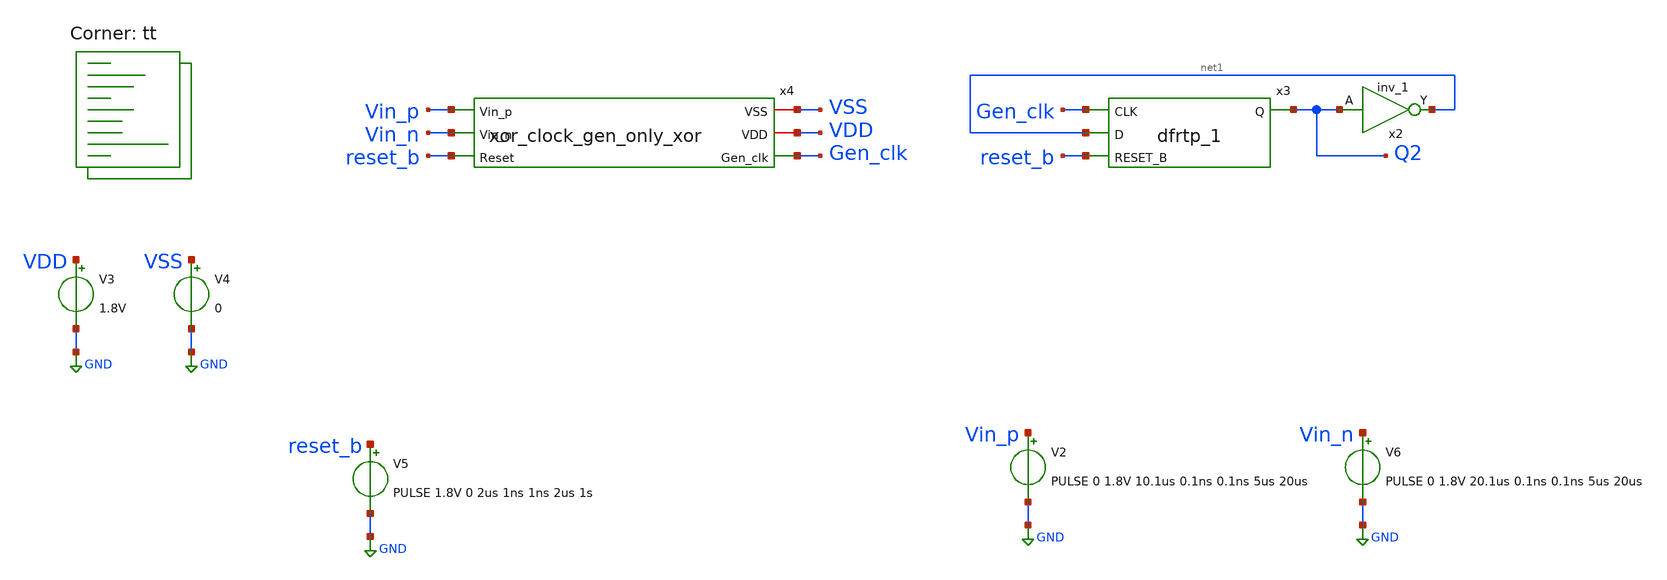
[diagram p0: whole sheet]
** sch_path: xschem/tests/xor_clock_gen/xor_clock_gen__only_xor_test.sch
**.subckt xor_clock_gen__only_xor_test
V3 VDD GND 1.8V
V4 VSS GND 0
V5 reset_b GND PULSE 1.8V 0 2us 1ns 1ns 2us 1s
V2 Vin_p GND PULSE 0 1.8V 10.1us 0.1ns 0.1ns 5us 20us
V6 Vin_n GND PULSE 0 1.8V 20.1us 0.1ns 0.1ns 5us 20us
x3 Gen_clk net1 reset_b VSS VSS VDD VDD Q2 sky130_fd_sc_hd__dfrtp_1
x2 Q2 VSS VSS VDD VDD net1 sky130_fd_sc_hd__inv_1
x4 VSS Vin_p VDD Vin_n Gen_clk reset_b xor_clock_gen_only_xor
**** begin user architecture code
 *.lib $::SKYWATER_MODELS/sky130.lib.spice tt
.include $::SKYWATER_STDCELLS/sky130_fd_sc_hd.spice


.options acct list
.temp 25
*vvcc VDD 0 dc 1.8
*vvss VSS 0 0
.control
save all
tran 0.01u 80u
*plot RST_PLS clk+2 Pulse+4
plot Vin_p-Vin_n reset_b-2 Gen_clk+2 Q2+4
write xor_clock_gen_only_xor_test.raw
.endc


.lib $::SKYWATER_MODELS/sky130.lib.spice tt
**** end user architecture code
**.ends

* expanding   symbol:  src/xor_clock_gen/xor_clock_gen_only_xor.sym # of pins=6
** sym_path: xschem/src/xor_clock_gen/xor_clock_gen_only_xor.sym
** sch_path: xschem/src/xor_clock_gen/xor_clock_gen_only_xor.sch
.subckt xor_clock_gen_only_xor VSS Vin_p VDD Vin_n Gen_clk Reset
*.ipin Vin_p
*.iopin VSS
*.opin Gen_clk
*.iopin VDD
*.ipin Vin_n
*.ipin Reset
x2 Vin_p Vin_n VSS VSS VDD VDD Gen_clk sky130_fd_sc_hd__xor2_1
.ends

.GLOBAL GND
.end
